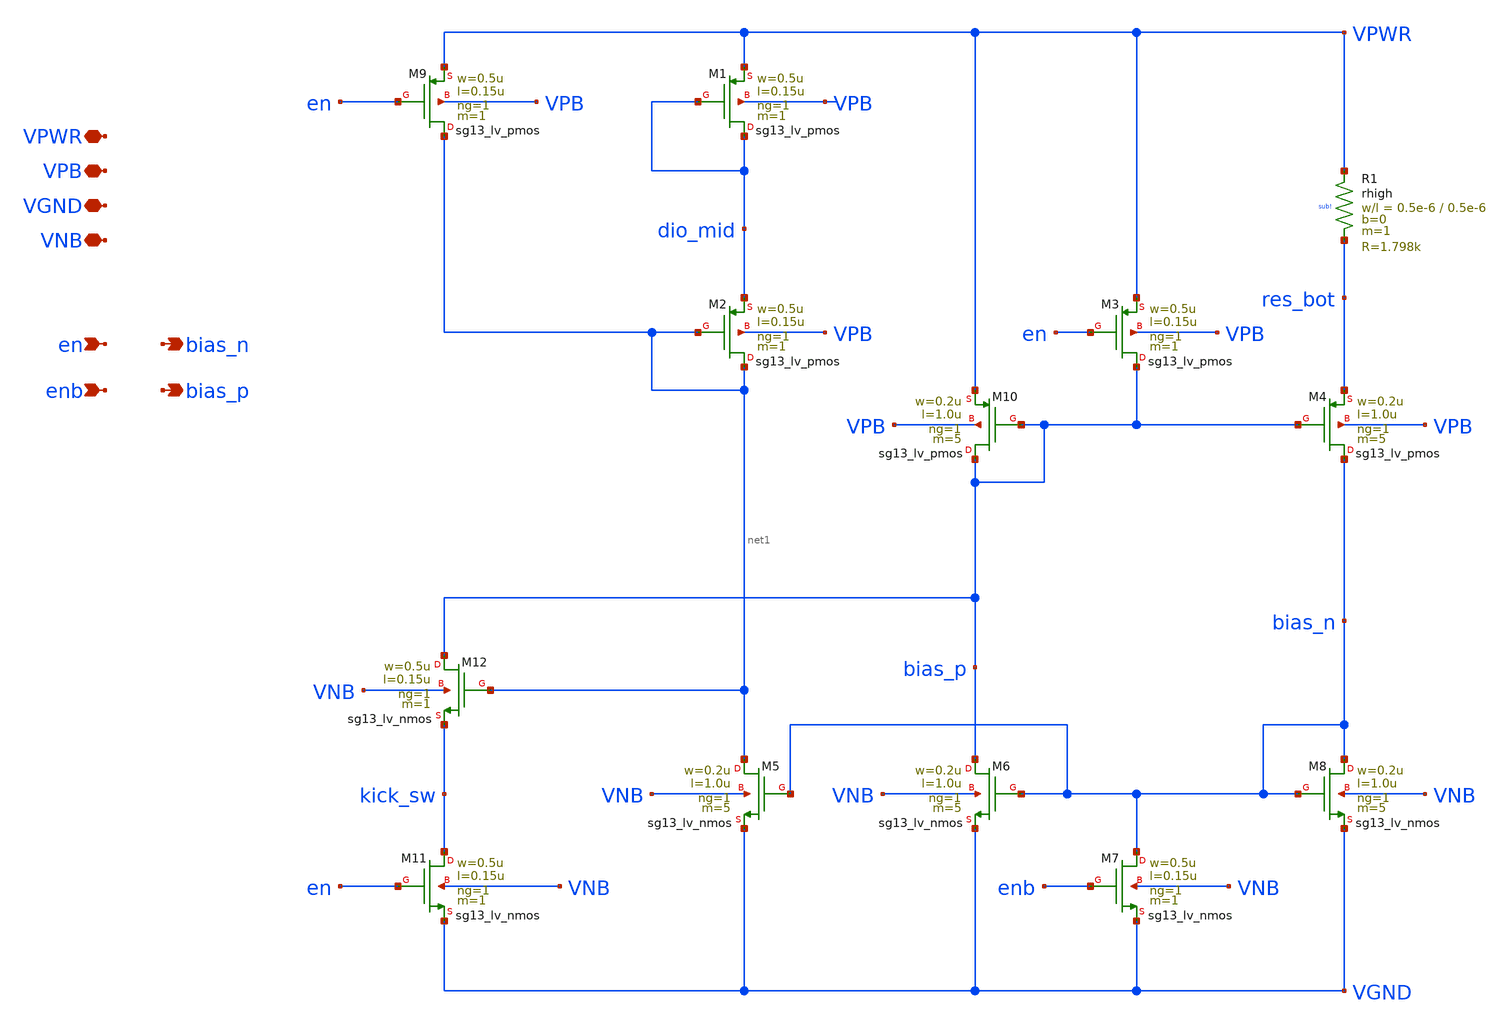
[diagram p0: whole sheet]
** sch_path: Team Designs/Team 2 Design/design_data/xschem/t2_bias.sch
**.subckt t2_bias VPWR VPB VGND VNB en enb bias_n bias_p
*.iopin VPWR
*.iopin VPB
*.iopin VGND
*.iopin VNB
*.ipin en
*.ipin enb
*.opin bias_n
*.opin bias_p
XM9 net1 en VPWR VPB sg13_lv_pmos w=0.5u l=0.15u ng=1 m=1 mm_ok=1
XM10 bias_p bias_p VPWR VPB sg13_lv_pmos w=0.2u l=1.0u ng=1 m=5 mm_ok=1
XM1 dio_mid dio_mid VPWR VPB sg13_lv_pmos w=0.5u l=0.15u ng=1 m=1 mm_ok=1
XM2 net1 net1 dio_mid VPB sg13_lv_pmos w=0.5u l=0.15u ng=1 m=1 mm_ok=1
XM3 bias_p en VPWR VPB sg13_lv_pmos w=0.5u l=0.15u ng=1 m=1 mm_ok=1
XM4 bias_n bias_p res_bot VPB sg13_lv_pmos w=0.2u l=1.0u ng=1 m=5 mm_ok=1
XM11 kick_sw en VGND VNB sg13_lv_nmos w=0.5u l=0.15u ng=1 m=1 mm_ok=1
XM12 bias_p net1 kick_sw VNB sg13_lv_nmos w=0.5u l=0.15u ng=1 m=1 mm_ok=1
XM5 net1 bias_n VGND VNB sg13_lv_nmos w=0.2u l=1.0u ng=1 m=5 mm_ok=1
XM6 bias_p bias_n VGND VNB sg13_lv_nmos w=0.2u l=1.0u ng=1 m=5 mm_ok=1
XM7 bias_n enb VGND VNB sg13_lv_nmos w=0.5u l=0.15u ng=1 m=1 mm_ok=1
XM8 bias_n bias_n VGND VNB sg13_lv_nmos w=0.2u l=1.0u ng=1 m=5 mm_ok=1
XR1 VPWR res_bot sub! rhigh w=0.5e-6 l=0.5e-6 m=1 b=0 mm_ok=1
**.ends
.end
